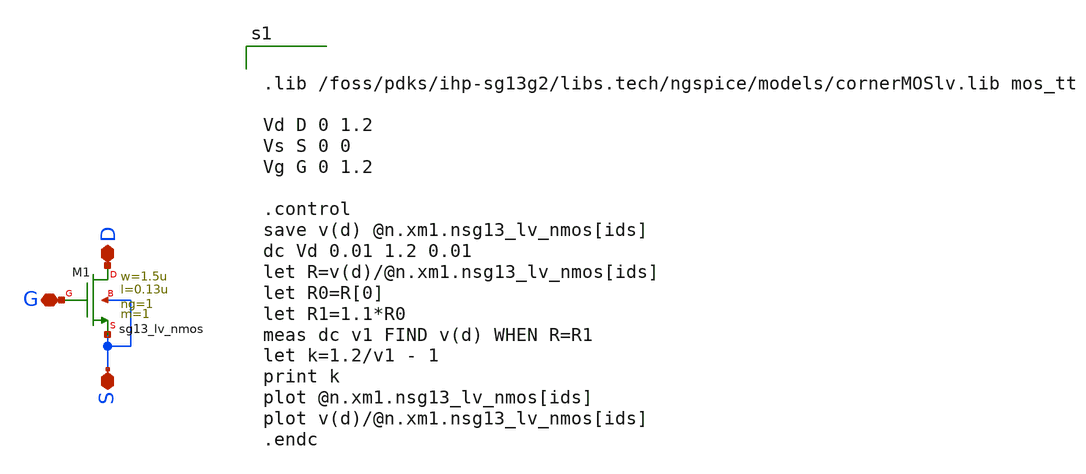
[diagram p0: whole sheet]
** sch_path: xschem/nmos_tb.sch
**.subckt nmos_tb S G D
*.iopin S
*.iopin G
*.iopin D
XM1 D G S S sg13_lv_nmos w=1.5u l=0.13u ng=1 m=1 mm_ok=1
**** begin user architecture code


.lib /foss/pdks/ihp-sg13g2/libs.tech/ngspice/models/cornerMOSlv.lib mos_tt

Vd D 0 1.2
Vs S 0 0
Vg G 0 1.2

.control
save v(d) @n.xm1.nsg13_lv_nmos[ids]
dc Vd 0.01 1.2 0.01
let R=v(d)/@n.xm1.nsg13_lv_nmos[ids]
let R0=R[0]
let R1=1.1*R0
meas dc v1 FIND v(d) WHEN R=R1
let k=1.2/v1 - 1
print k
plot @n.xm1.nsg13_lv_nmos[ids]
plot v(d)/@n.xm1.nsg13_lv_nmos[ids]
.endc


**** end user architecture code
**.ends
.end
